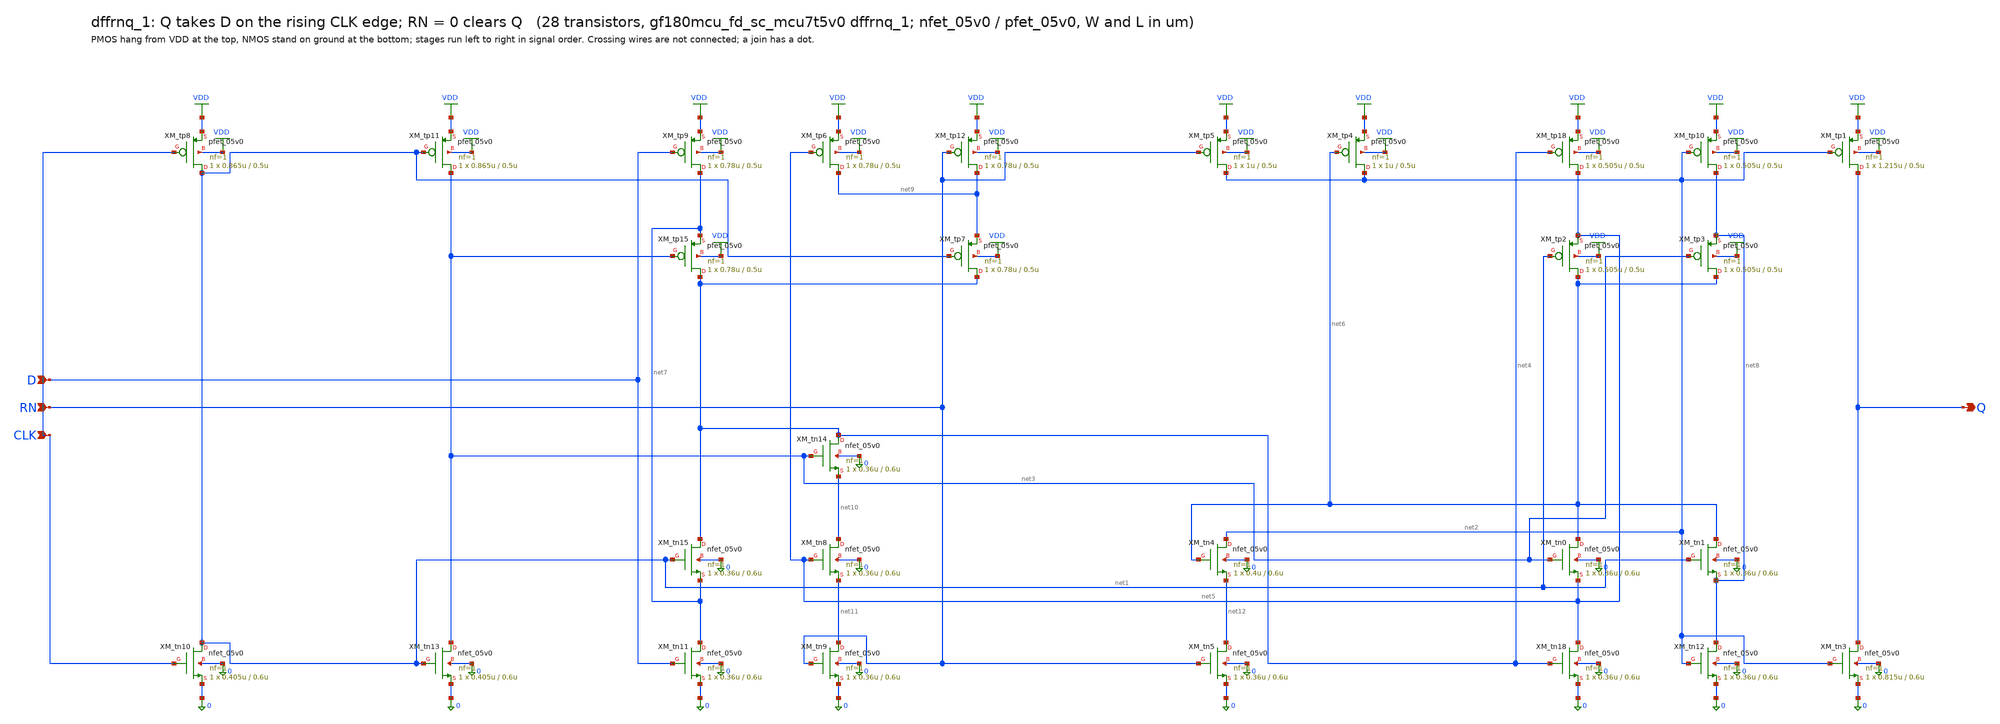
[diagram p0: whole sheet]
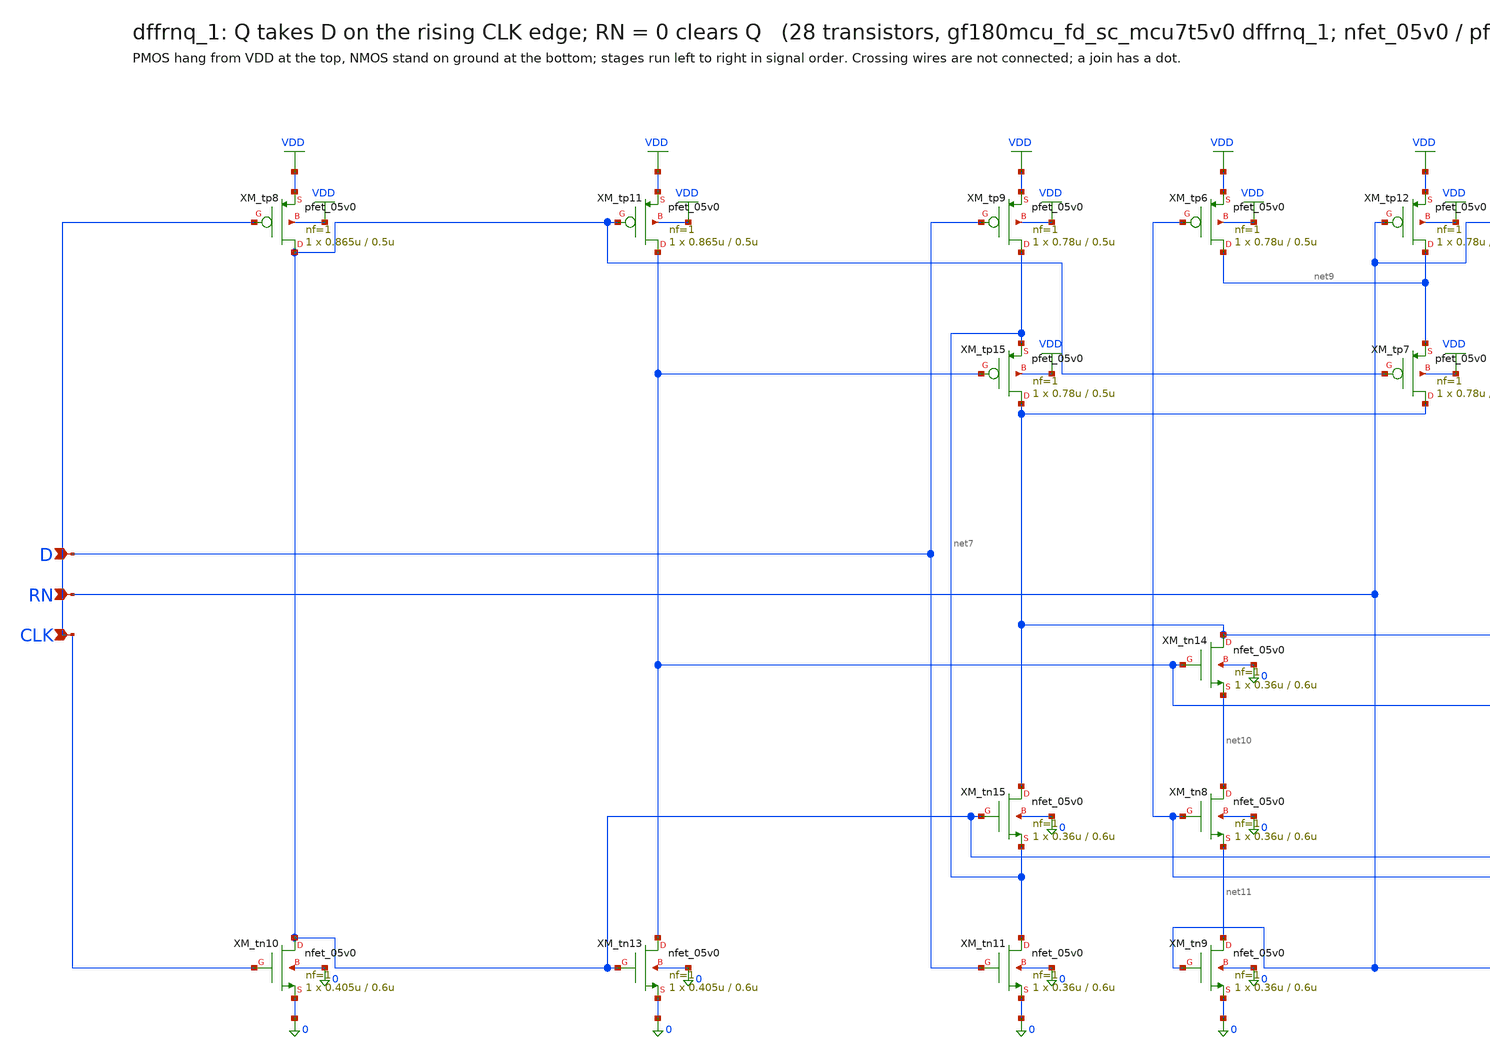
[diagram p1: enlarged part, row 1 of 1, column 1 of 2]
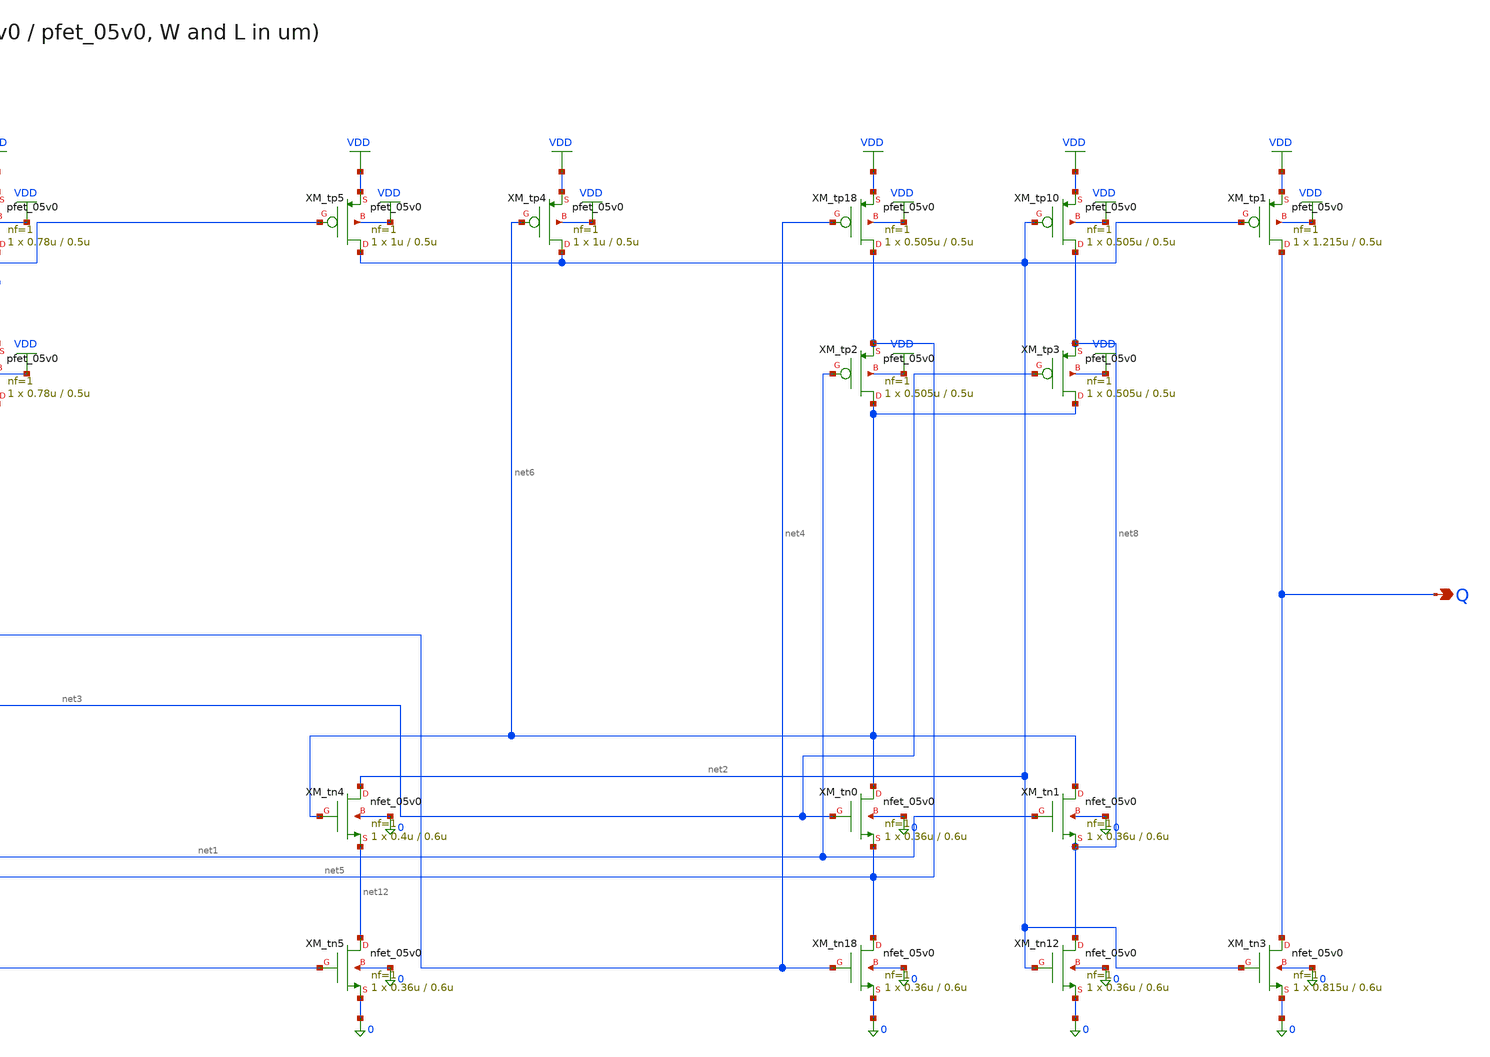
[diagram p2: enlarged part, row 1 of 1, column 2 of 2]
** sch_path: xschem/cells_tx/dffrnq_1.sch
**.subckt dffrnq_1 D RN CLK Q
*.ipin D
*.ipin RN
*.ipin CLK
*.opin Q
XM_tn10 net1 CLK 0 0 nfet_05v0 L=0.6u W=0.405u nf=1 ad=2.025e-13 as=2.025e-13 pd=1.81e-06
+ ps=1.81e-06 nrd=0 nrs=0 sa=0 sb=0 sd=0 m=1
XM_tn13 net3 net1 0 0 nfet_05v0 L=0.6u W=0.405u nf=1 ad=2.025e-13 as=2.025e-13 pd=1.81e-06
+ ps=1.81e-06 nrd=0 nrs=0 sa=0 sb=0 sd=0 m=1
XM_tn11 net7 D 0 0 nfet_05v0 L=0.6u W=0.36u nf=1 ad=1.8e-13 as=1.8e-13 pd=1.72e-06 ps=1.72e-06 nrd=0
+ nrs=0 sa=0 sb=0 sd=0 m=1
XM_tn15 net4 net1 net7 0 nfet_05v0 L=0.6u W=0.36u nf=1 ad=1.8e-13 as=1.8e-13 pd=1.72e-06 ps=1.72e-06
+ nrd=0 nrs=0 sa=0 sb=0 sd=0 m=1
XM_tn14 net4 net3 net10 0 nfet_05v0 L=0.6u W=0.36u nf=1 ad=1.8e-13 as=1.8e-13 pd=1.72e-06
+ ps=1.72e-06 nrd=0 nrs=0 sa=0 sb=0 sd=0 m=1
XM_tn8 net10 net5 net11 0 nfet_05v0 L=0.6u W=0.36u nf=1 ad=1.8e-13 as=1.8e-13 pd=1.72e-06
+ ps=1.72e-06 nrd=0 nrs=0 sa=0 sb=0 sd=0 m=1
XM_tn9 net11 RN 0 0 nfet_05v0 L=0.6u W=0.36u nf=1 ad=1.8e-13 as=1.8e-13 pd=1.72e-06 ps=1.72e-06
+ nrd=0 nrs=0 sa=0 sb=0 sd=0 m=1
XM_tn18 net5 net4 0 0 nfet_05v0 L=0.6u W=0.36u nf=1 ad=1.8e-13 as=1.8e-13 pd=1.72e-06 ps=1.72e-06
+ nrd=0 nrs=0 sa=0 sb=0 sd=0 m=1
XM_tn0 net6 net3 net5 0 nfet_05v0 L=0.6u W=0.36u nf=1 ad=1.8e-13 as=1.8e-13 pd=1.72e-06 ps=1.72e-06
+ nrd=0 nrs=0 sa=0 sb=0 sd=0 m=1
XM_tn1 net6 net1 net8 0 nfet_05v0 L=0.6u W=0.36u nf=1 ad=1.8e-13 as=1.8e-13 pd=1.72e-06 ps=1.72e-06
+ nrd=0 nrs=0 sa=0 sb=0 sd=0 m=1
XM_tn12 net8 net2 0 0 nfet_05v0 L=0.6u W=0.36u nf=1 ad=1.8e-13 as=1.8e-13 pd=1.72e-06 ps=1.72e-06
+ nrd=0 nrs=0 sa=0 sb=0 sd=0 m=1
XM_tn5 net12 RN 0 0 nfet_05v0 L=0.6u W=0.36u nf=1 ad=1.8e-13 as=1.8e-13 pd=1.72e-06 ps=1.72e-06
+ nrd=0 nrs=0 sa=0 sb=0 sd=0 m=1
XM_tn4 net2 net6 net12 0 nfet_05v0 L=0.6u W=0.4u nf=1 ad=2e-13 as=2e-13 pd=1.8e-06 ps=1.8e-06 nrd=0
+ nrs=0 sa=0 sb=0 sd=0 m=1
XM_tn3 Q net2 0 0 nfet_05v0 L=0.6u W=0.815u nf=1 ad=4.075e-13 as=4.075e-13 pd=2.63e-06 ps=2.63e-06
+ nrd=0 nrs=0 sa=0 sb=0 sd=0 m=1
XM_tp8 net1 CLK VDD VDD pfet_05v0 L=0.5u W=0.865u nf=1 ad=4.325e-13 as=4.325e-13 pd=2.73e-06
+ ps=2.73e-06 nrd=0 nrs=0 sa=0 sb=0 sd=0 m=1
XM_tp11 net3 net1 VDD VDD pfet_05v0 L=0.5u W=0.865u nf=1 ad=4.325e-13 as=4.325e-13 pd=2.73e-06
+ ps=2.73e-06 nrd=0 nrs=0 sa=0 sb=0 sd=0 m=1
XM_tp9 net7 D VDD VDD pfet_05v0 L=0.5u W=0.78u nf=1 ad=3.9e-13 as=3.9e-13 pd=2.56e-06 ps=2.56e-06
+ nrd=0 nrs=0 sa=0 sb=0 sd=0 m=1
XM_tp15 net4 net3 net7 VDD pfet_05v0 L=0.5u W=0.78u nf=1 ad=3.9e-13 as=3.9e-13 pd=2.56e-06
+ ps=2.56e-06 nrd=0 nrs=0 sa=0 sb=0 sd=0 m=1
XM_tp7 net4 net1 net9 VDD pfet_05v0 L=0.5u W=0.78u nf=1 ad=3.9e-13 as=3.9e-13 pd=2.56e-06
+ ps=2.56e-06 nrd=0 nrs=0 sa=0 sb=0 sd=0 m=1
XM_tp6 net9 net5 VDD VDD pfet_05v0 L=0.5u W=0.78u nf=1 ad=3.9e-13 as=3.9e-13 pd=2.56e-06 ps=2.56e-06
+ nrd=0 nrs=0 sa=0 sb=0 sd=0 m=1
XM_tp12 net9 RN VDD VDD pfet_05v0 L=0.5u W=0.78u nf=1 ad=3.9e-13 as=3.9e-13 pd=2.56e-06 ps=2.56e-06
+ nrd=0 nrs=0 sa=0 sb=0 sd=0 m=1
XM_tp18 net5 net4 VDD VDD pfet_05v0 L=0.5u W=0.505u nf=1 ad=2.525e-13 as=2.525e-13 pd=2.01e-06
+ ps=2.01e-06 nrd=0 nrs=0 sa=0 sb=0 sd=0 m=1
XM_tp2 net6 net1 net5 VDD pfet_05v0 L=0.5u W=0.505u nf=1 ad=2.525e-13 as=2.525e-13 pd=2.01e-06
+ ps=2.01e-06 nrd=0 nrs=0 sa=0 sb=0 sd=0 m=1
XM_tp3 net6 net3 net8 VDD pfet_05v0 L=0.5u W=0.505u nf=1 ad=2.525e-13 as=2.525e-13 pd=2.01e-06
+ ps=2.01e-06 nrd=0 nrs=0 sa=0 sb=0 sd=0 m=1
XM_tp10 net8 net2 VDD VDD pfet_05v0 L=0.5u W=0.505u nf=1 ad=2.525e-13 as=2.525e-13 pd=2.01e-06
+ ps=2.01e-06 nrd=0 nrs=0 sa=0 sb=0 sd=0 m=1
XM_tp5 net2 RN VDD VDD pfet_05v0 L=0.5u W=1u nf=1 ad=5e-13 as=5e-13 pd=3e-06 ps=3e-06 nrd=0 nrs=0
+ sa=0 sb=0 sd=0 m=1
XM_tp4 net2 net6 VDD VDD pfet_05v0 L=0.5u W=1u nf=1 ad=5e-13 as=5e-13 pd=3e-06 ps=3e-06 nrd=0 nrs=0
+ sa=0 sb=0 sd=0 m=1
XM_tp1 Q net2 VDD VDD pfet_05v0 L=0.5u W=1.215u nf=1 ad=6.075e-13 as=6.075e-13 pd=3.43e-06
+ ps=3.43e-06 nrd=0 nrs=0 sa=0 sb=0 sd=0 m=1
**.ends
.GLOBAL VDD
.end
